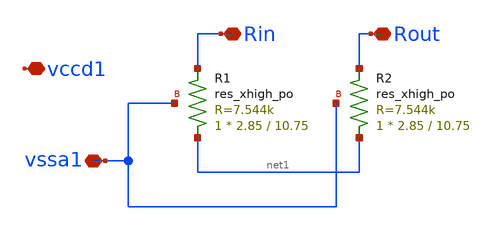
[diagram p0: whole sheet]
** sch_path: xschem/xschem/analog_stdcells/skywater_asc_res_xhigh_po_2p85_2.sch
**.subckt skywater_asc_res_xhigh_po_2p85_2 Rin Rout vccd1 vssa1
*.iopin Rin
*.iopin Rout
*.iopin vccd1
*.iopin vssa1
XR1 net1 Rin vssa1 sky130_fd_pr__res_xhigh_po W=2.85 L=10.75 mult=1 m=1
XR2 net1 Rout vssa1 sky130_fd_pr__res_xhigh_po W=2.85 L=10.75 mult=1 m=1
**.ends
.end
